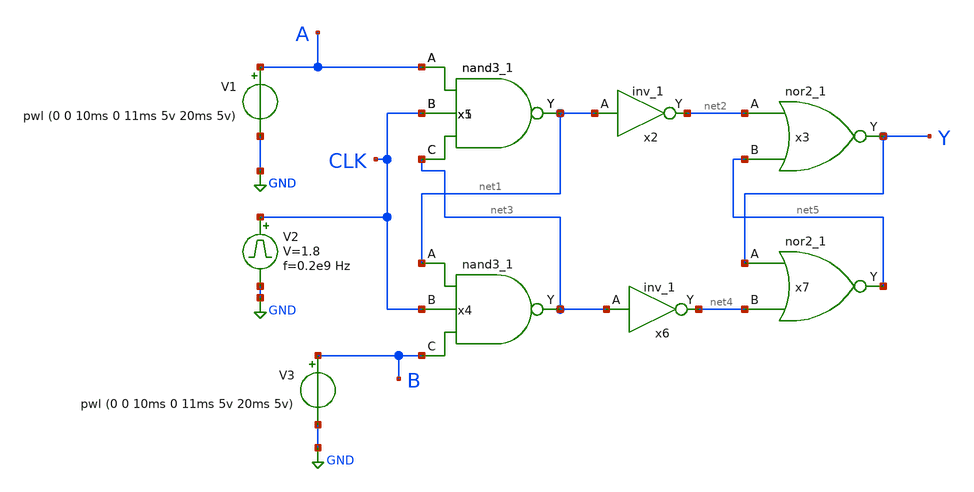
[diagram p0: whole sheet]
** sch_path: analog comparator/comparator.sch
**.subckt comparator
x1 A CLK net3 VSS VSS VCC VCC net1 sky130_fd_sc_hd__nand3_1
V1 A GND pwl (0 0 10ms 0 11ms 5v 20ms 5v)
x2 net1 VSS VSS VCC VCC net2 sky130_fd_sc_hd__inv_1
x3 net2 net5 VSS VSS VCC VCC Y sky130_fd_sc_hd__nor2_1
x4 net1 CLK B VSS VSS VCC VCC net3 sky130_fd_sc_hd__nand3_1
x5 A CLK net3 VSS VSS VCC VCC net1 sky130_fd_sc_hd__nand3_1
x6 net3 VSS VSS VCC VCC net4 sky130_fd_sc_hd__inv_1
x7 Y net4 VSS VSS VCC VCC net5 sky130_fd_sc_hd__nor2_1
V2 CLK GND pulse 0 1.8 '0.495/ 0.2e9 ' '0.01/0.2e9 ' '0.01/0.2e9 ' '0.49/0.2e9 ' '1/0.2e9 '
V3 B GND pwl (0 0 10ms 0 11ms 5v 20ms 5v)
**** begin user architecture code


.temp 25
vvcc vcc 0 dc 1.8
vvss vss 0 0
.control
tran 30p 80n
plot A B Y
.endc



.include $::SKYWATER_MODELS/cells/nfet_01v8/sky130_fd_pr__nfet_01v8__tt.corner.spice
.include $::SKYWATER_MODELS/cells/nfet_01v8_lvt/sky130_fd_pr__nfet_01v8_lvt__tt.corner.spice
.include $::SKYWATER_MODELS/cells/pfet_01v8/sky130_fd_pr__pfet_01v8__tt.corner.spice
.include $::SKYWATER_MODELS/cells/nfet_03v3_nvt/sky130_fd_pr__nfet_03v3_nvt__tt.corner.spice
.include $::SKYWATER_MODELS/cells/nfet_05v0_nvt/sky130_fd_pr__nfet_05v0_nvt__tt.corner.spice
.include $::SKYWATER_MODELS/cells/esd_nfet_01v8/sky130_fd_pr__esd_nfet_01v8__tt.corner.spice
.include $::SKYWATER_MODELS/cells/pfet_01v8_lvt/sky130_fd_pr__pfet_01v8_lvt__tt.corner.spice
.include $::SKYWATER_MODELS/cells/pfet_01v8_hvt/sky130_fd_pr__pfet_01v8_hvt__tt.corner.spice
.include $::SKYWATER_MODELS/cells/esd_pfet_g5v0d10v5/sky130_fd_pr__esd_pfet_g5v0d10v5__tt.corner.spice
.include $::SKYWATER_MODELS/cells/pfet_g5v0d10v5/sky130_fd_pr__pfet_g5v0d10v5__tt.corner.spice
.include $::SKYWATER_MODELS/cells/pfet_g5v0d16v0/sky130_fd_pr__pfet_g5v0d16v0__tt.corner.spice
.include $::SKYWATER_MODELS/cells/nfet_g5v0d10v5/sky130_fd_pr__nfet_g5v0d10v5__tt.corner.spice
.include $::SKYWATER_MODELS/cells/nfet_g5v0d16v0/sky130_fd_pr__nfet_g5v0d16v0__tt_discrete.corner.spice
.include $::SKYWATER_MODELS/cells/esd_nfet_g5v0d10v5/sky130_fd_pr__esd_nfet_g5v0d10v5__tt.corner.spice
.include $::SKYWATER_MODELS/models/corners/tt/nonfet.spice
* Mismatch parameters
.include $::SKYWATER_MODELS/cells/nfet_01v8/sky130_fd_pr__nfet_01v8__mismatch.corner.spice
.include $::SKYWATER_MODELS/cells/pfet_01v8/sky130_fd_pr__pfet_01v8__mismatch.corner.spice
.include $::SKYWATER_MODELS/cells/nfet_01v8_lvt/sky130_fd_pr__nfet_01v8_lvt__mismatch.corner.spice
.include $::SKYWATER_MODELS/cells/pfet_01v8_lvt/sky130_fd_pr__pfet_01v8_lvt__mismatch.corner.spice
.include $::SKYWATER_MODELS/cells/pfet_01v8_hvt/sky130_fd_pr__pfet_01v8_hvt__mismatch.corner.spice
.include $::SKYWATER_MODELS/cells/nfet_g5v0d10v5/sky130_fd_pr__nfet_g5v0d10v5__mismatch.corner.spice
.include $::SKYWATER_MODELS/cells/pfet_g5v0d10v5/sky130_fd_pr__pfet_g5v0d10v5__mismatch.corner.spice
.include $::SKYWATER_MODELS/cells/nfet_05v0_nvt/sky130_fd_pr__nfet_05v0_nvt__mismatch.corner.spice
.include $::SKYWATER_MODELS/cells/nfet_03v3_nvt/sky130_fd_pr__nfet_03v3_nvt__mismatch.corner.spice
* Resistor$::SKYWATER_MODELS/Capacitor
.include $::SKYWATER_MODELS/models/r+c/res_typical__cap_typical.spice
.include $::SKYWATER_MODELS/models/r+c/res_typical__cap_typical__lin.spice
* Special cells
.include $::SKYWATER_MODELS/models/corners/tt/specialized_cells.spice
* All models
.include $::SKYWATER_MODELS/models/all.spice
* Corner
.include $::SKYWATER_MODELS/models/corners/tt/rf.spice

**** end user architecture code
**.ends
.GLOBAL GND
**** begin user architecture code
[sky130_models]
**** end user architecture code
.end
